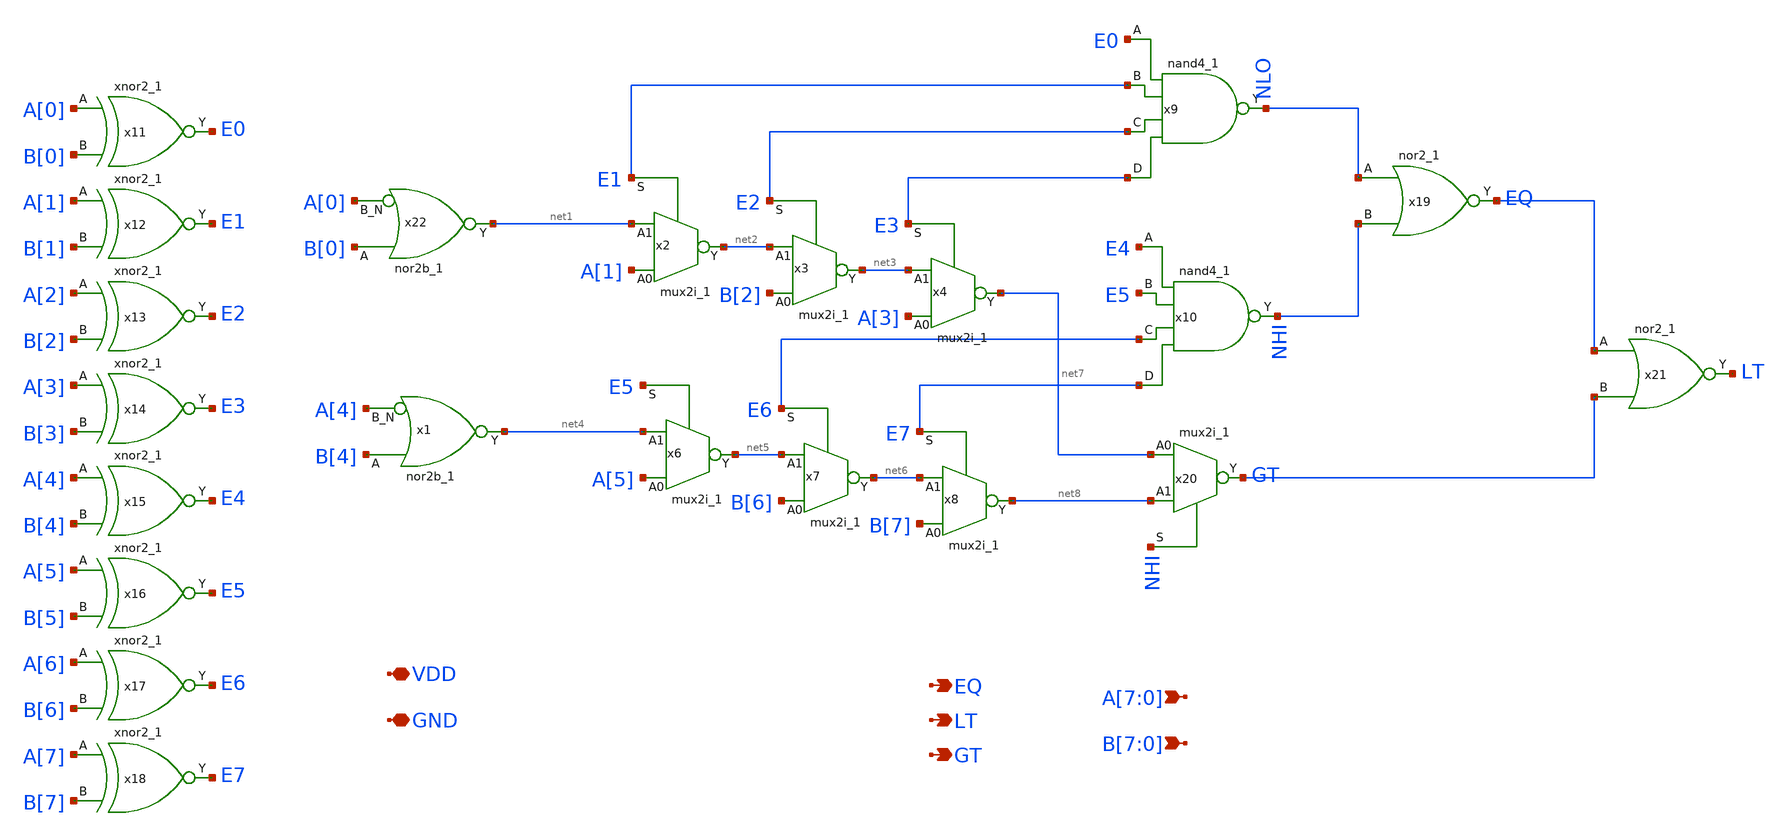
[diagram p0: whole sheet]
** sch_path: xschem/comparator_8bit.sch
**.subckt comparator_8bit EQ LT GT VDD GND A[7],A[6],A[5],A[4],A[3],A[2],A[1],A[0]
*+ B[7],B[6],B[5],B[4],B[3],B[2],B[1],B[0]
*.opin EQ
*.opin LT
*.opin GT
*.iopin VDD
*.iopin GND
*.ipin A[7],A[6],A[5],A[4],A[3],A[2],A[1],A[0]
*.ipin B[7],B[6],B[5],B[4],B[3],B[2],B[1],B[0]
x2 A[1] net1 E1 GND GND VDD VDD net2 sky130_fd_sc_hd__mux2i_1
x3 B[2] net2 E2 GND GND VDD VDD net3 sky130_fd_sc_hd__mux2i_1
x4 A[3] net3 E3 GND GND VDD VDD net7 sky130_fd_sc_hd__mux2i_1
x6 A[5] net4 E5 GND GND VDD VDD net5 sky130_fd_sc_hd__mux2i_1
x7 B[6] net5 E6 GND GND VDD VDD net6 sky130_fd_sc_hd__mux2i_1
x8 B[7] net6 E7 GND GND VDD VDD net8 sky130_fd_sc_hd__mux2i_1
x9 E0 E1 E2 E3 GND GND VDD VDD NLO sky130_fd_sc_hd__nand4_1
x11 A[0] B[0] GND GND VDD VDD E0 sky130_fd_sc_hd__xnor2_1
x10 E4 E5 E6 E7 GND GND VDD VDD NHI sky130_fd_sc_hd__nand4_1
x19 NLO NHI GND GND VDD VDD EQ sky130_fd_sc_hd__nor2_1
x20 net7 net8 NHI GND GND VDD VDD GT sky130_fd_sc_hd__mux2i_1
x21 EQ GT GND GND VDD VDD LT sky130_fd_sc_hd__nor2_1
x12 A[1] B[1] GND GND VDD VDD E1 sky130_fd_sc_hd__xnor2_1
x13 A[2] B[2] GND GND VDD VDD E2 sky130_fd_sc_hd__xnor2_1
x14 A[3] B[3] GND GND VDD VDD E3 sky130_fd_sc_hd__xnor2_1
x15 A[4] B[4] GND GND VDD VDD E4 sky130_fd_sc_hd__xnor2_1
x16 A[5] B[5] GND GND VDD VDD E5 sky130_fd_sc_hd__xnor2_1
x17 A[6] B[6] GND GND VDD VDD E6 sky130_fd_sc_hd__xnor2_1
x18 A[7] B[7] GND GND VDD VDD E7 sky130_fd_sc_hd__xnor2_1
x22 B[0] A[0] GND GND VDD VDD net1 sky130_fd_sc_hd__nor2b_1
x1 B[4] A[4] GND GND VDD VDD net4 sky130_fd_sc_hd__nor2b_1
**.ends
.end
